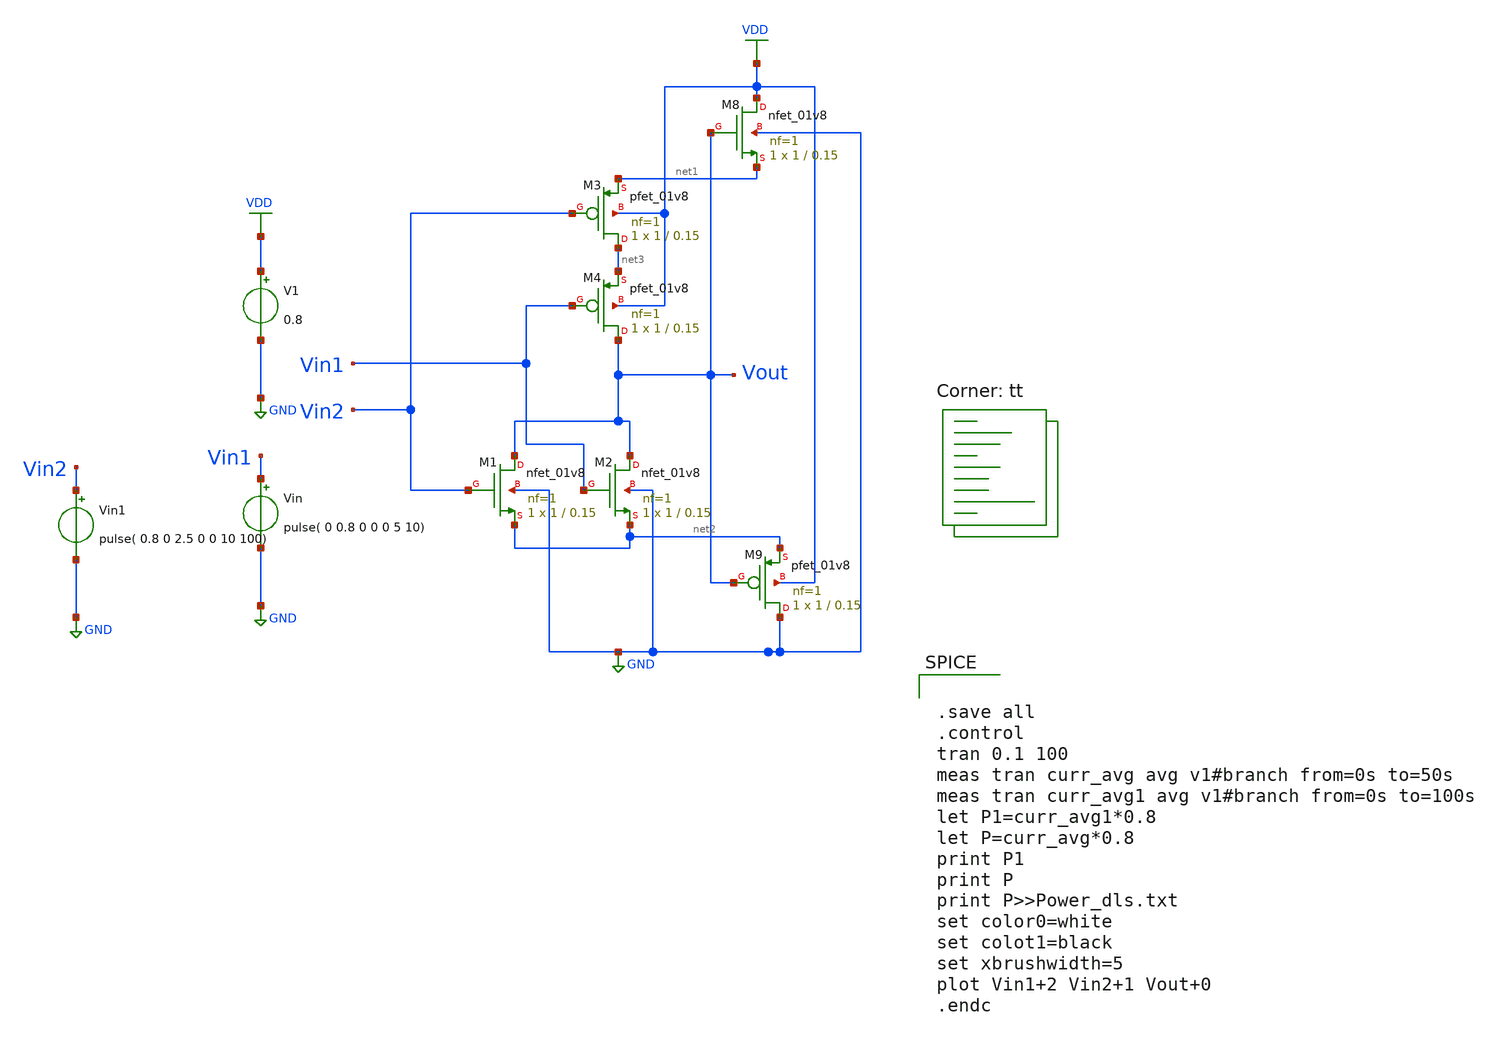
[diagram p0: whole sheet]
** sch_path: dls_nor.sch
**.subckt dls_nor
V1 VDD GND 0.8
Vin Vin1 GND pulse( 0 0.8 0 0 0 5 10)
XM8 VDD Vout net1 GND sky130_fd_pr__nfet_01v8 L=0.15 W=1 nf=1 ad='int((nf+1)/2) * W/nf * 0.29' as='int((nf+2)/2) * W/nf * 0.29'
+ pd='2*int((nf+1)/2) * (W/nf + 0.29)' ps='2*int((nf+2)/2) * (W/nf + 0.29)' nrd='0.29 / W' nrs='0.29 / W'
+ sa=0 sb=0 sd=0 mult=1 m=1
XM9 GND Vout net2 VDD sky130_fd_pr__pfet_01v8 L=0.15 W=1 nf=1 ad='int((nf+1)/2) * W/nf * 0.29' as='int((nf+2)/2) * W/nf * 0.29'
+ pd='2*int((nf+1)/2) * (W/nf + 0.29)' ps='2*int((nf+2)/2) * (W/nf + 0.29)' nrd='0.29 / W' nrs='0.29 / W'
+ sa=0 sb=0 sd=0 mult=1 m=1
Vin1 Vin2 GND pulse( 0.8 0 2.5 0 0 10 100)
XM1 Vout Vin2 net2 GND sky130_fd_pr__nfet_01v8 L=0.15 W=1 nf=1 ad='int((nf+1)/2) * W/nf * 0.29' as='int((nf+2)/2) * W/nf * 0.29'
+ pd='2*int((nf+1)/2) * (W/nf + 0.29)' ps='2*int((nf+2)/2) * (W/nf + 0.29)' nrd='0.29 / W' nrs='0.29 / W'
+ sa=0 sb=0 sd=0 mult=1 m=1
XM2 Vout Vin1 net2 GND sky130_fd_pr__nfet_01v8 L=0.15 W=1 nf=1 ad='int((nf+1)/2) * W/nf * 0.29' as='int((nf+2)/2) * W/nf * 0.29'
+ pd='2*int((nf+1)/2) * (W/nf + 0.29)' ps='2*int((nf+2)/2) * (W/nf + 0.29)' nrd='0.29 / W' nrs='0.29 / W'
+ sa=0 sb=0 sd=0 mult=1 m=1
XM3 net3 Vin2 net1 VDD sky130_fd_pr__pfet_01v8 L=0.15 W=1 nf=1 ad='int((nf+1)/2) * W/nf * 0.29' as='int((nf+2)/2) * W/nf * 0.29'
+ pd='2*int((nf+1)/2) * (W/nf + 0.29)' ps='2*int((nf+2)/2) * (W/nf + 0.29)' nrd='0.29 / W' nrs='0.29 / W'
+ sa=0 sb=0 sd=0 mult=1 m=1
XM4 Vout Vin1 net3 VDD sky130_fd_pr__pfet_01v8 L=0.15 W=1 nf=1 ad='int((nf+1)/2) * W/nf * 0.29' as='int((nf+2)/2) * W/nf * 0.29'
+ pd='2*int((nf+1)/2) * (W/nf + 0.29)' ps='2*int((nf+2)/2) * (W/nf + 0.29)' nrd='0.29 / W' nrs='0.29 / W'
+ sa=0 sb=0 sd=0 mult=1 m=1
**** begin user architecture code
.lib $::SKYWATER_MODELS/sky130.lib.spice tt


.save all
.control
tran 0.1 100
meas tran curr_avg avg v1#branch from=0s to=50s
meas tran curr_avg1 avg v1#branch from=0s to=100s
let P1=curr_avg1*0.8
let P=curr_avg*0.8
print P1
print P
print P>>Power_dls.txt
set color0=white
set colot1=black
set xbrushwidth=5
plot Vin1+2 Vin2+1 Vout+0
.endc



**** end user architecture code
**.ends
.GLOBAL GND
.GLOBAL VDD
.end
